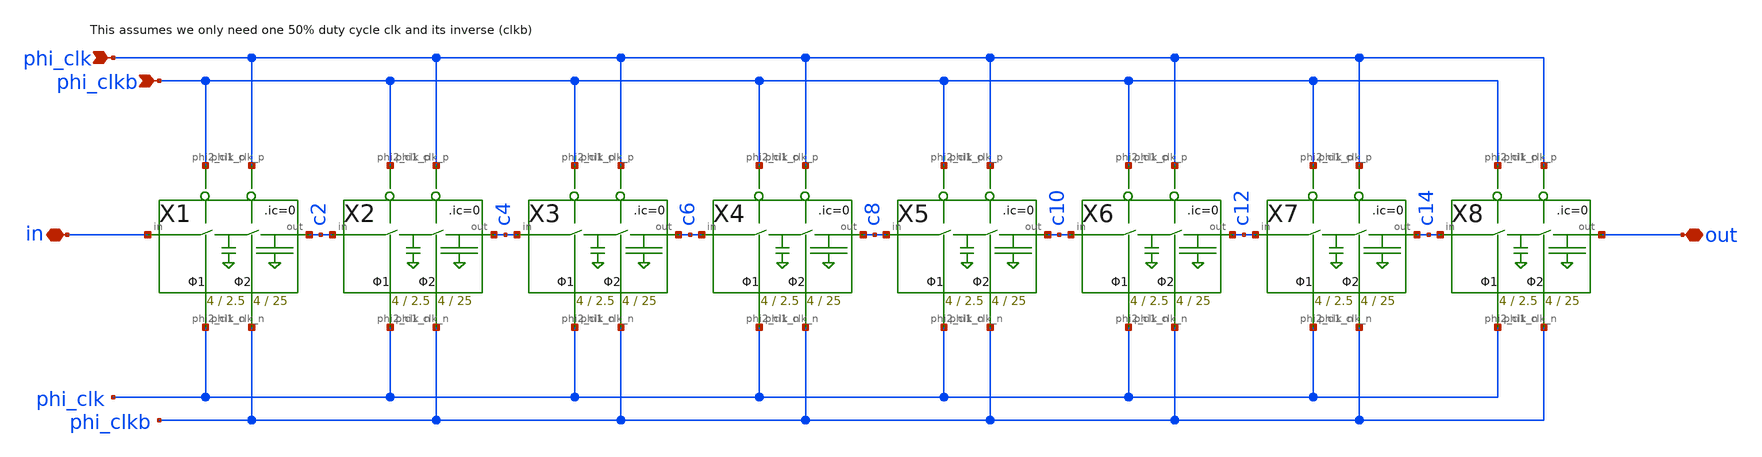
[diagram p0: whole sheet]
** sch_path: xschem/Switched_Caps/archive/16switchcaps.sch
**.subckt 16switchcaps in out phi_clk phi_clkb
*.iopin in
*.iopin out
*.ipin phi_clk
*.ipin phi_clkb
X1 in c2 phi_clkb phi_clk phi_clkb phi_clk 2switchcaps Wcap1=4 Lcap1=2.5 Wcap2=4 Lcap2=25
X2 c2 c4 phi_clkb phi_clk phi_clkb phi_clk 2switchcaps Wcap1=4 Lcap1=2.5 Wcap2=4 Lcap2=25
X3 c4 c6 phi_clkb phi_clk phi_clkb phi_clk 2switchcaps Wcap1=4 Lcap1=2.5 Wcap2=4 Lcap2=25
X4 c6 c8 phi_clkb phi_clk phi_clkb phi_clk 2switchcaps Wcap1=4 Lcap1=2.5 Wcap2=4 Lcap2=25
X5 c8 c10 phi_clkb phi_clk phi_clkb phi_clk 2switchcaps Wcap1=4 Lcap1=2.5 Wcap2=4 Lcap2=25
X6 c10 c12 phi_clkb phi_clk phi_clkb phi_clk 2switchcaps Wcap1=4 Lcap1=2.5 Wcap2=4 Lcap2=25
X7 c12 c14 phi_clkb phi_clk phi_clkb phi_clk 2switchcaps Wcap1=4 Lcap1=2.5 Wcap2=4 Lcap2=25
X8 c14 out phi_clkb phi_clk phi_clkb phi_clk 2switchcaps Wcap1=4 Lcap1=2.5 Wcap2=4 Lcap2=25
**.ends

* expanding   symbol:  Switched_Caps/2switchcaps.sym # of pins=6
** sym_path: xschem/Switched_Caps/2switchcaps.sym
** sch_path: xschem/Switched_Caps/2switchcaps.sch
.subckt 2switchcaps in out phi2_clk_n phi1_clk_n phi1_clk_p phi2_clk_p  Wcap1=4 Lcap1=2.5 Wcap2=4
+ Lcap2=25
*.iopin out
*.iopin in
*.ipin phi1_clk_n
*.ipin phi1_clk_p
*.ipin phi2_clk_p
*.ipin phi2_clk_n
XC1 c1 GND sky130_fd_pr__cap_mim_m3_1 W=Wcap1 L=Lcap1 MF=1 m=1
XC2 out GND sky130_fd_pr__cap_mim_m3_1 W=Wcap2 L=Lcap2 MF=1 m=1
**** begin user architecture code

.ic v(c1)=0 v(out)=0

**** end user architecture code
X1 in c1 phi1_clk_p phi1_clk_n transmission_gate Wpmos=0.42 Lpmos=0.18 Wnmos=0.42 Lnmos=0.18
X2 c1 out phi2_clk_p phi2_clk_n transmission_gate Wpmos=0.42 Lpmos=0.18 Wnmos=0.42 Lnmos=0.18
.ends


* expanding   symbol:  transmission_gate/transmission_gate.sym # of pins=4
** sym_path: xschem/transmission_gate/transmission_gate.sym
** sch_path: xschem/transmission_gate/transmission_gate.sch
.subckt transmission_gate in out ctrl_ ctrl  Wpmos=0.42 Lpmos=0.18 Wnmos=0.42 Lnmos=0.18
*.iopin in
*.iopin out
*.ipin ctrl_
*.ipin ctrl
XM1 out ctrl in GND sky130_fd_pr__nfet_01v8 L=Lnmos W=Wnmos nf=1 ad='int((nf+1)/2) * W/nf * 0.29' as='int((nf+2)/2) * W/nf * 0.29'
+ pd='2*int((nf+1)/2) * (W/nf + 0.29)' ps='2*int((nf+2)/2) * (W/nf + 0.29)' nrd='0.29 / W' nrs='0.29 / W'
+ sa=0 sb=0 sd=0 mult=1 m=1
XM2 out ctrl_ in VDD sky130_fd_pr__pfet_01v8 L=Lpmos W=Wpmos nf=1 ad='int((nf+1)/2) * W/nf * 0.29' as='int((nf+2)/2) * W/nf * 0.29'
+ pd='2*int((nf+1)/2) * (W/nf + 0.29)' ps='2*int((nf+2)/2) * (W/nf + 0.29)' nrd='0.29 / W' nrs='0.29 / W'
+ sa=0 sb=0 sd=0 mult=1 m=1
.ends

.GLOBAL GND
.GLOBAL VDD
.end
